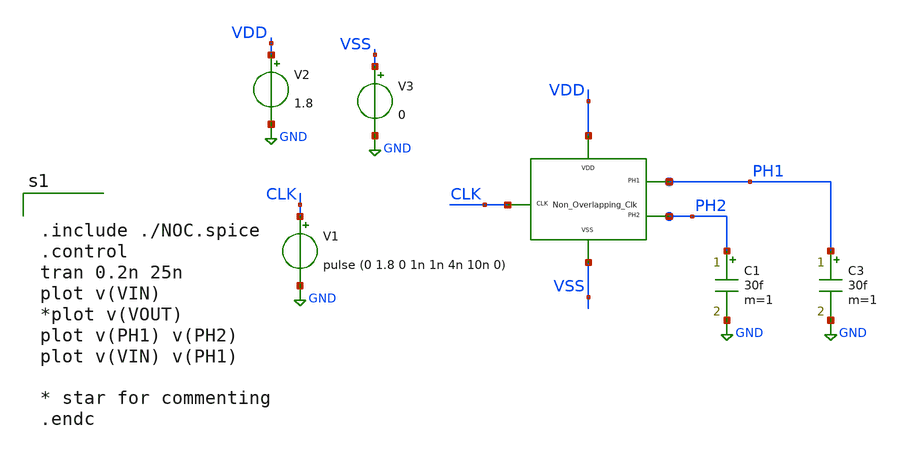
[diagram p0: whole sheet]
** sch_path: xschem/DC_DC_Converter_xschem/DC_DC_Converter/Non_Overlap_Clk/Non_over_clk_PEX_TB.sch
**.subckt Non_over_clk_PEX_TB
V1 CLK GND pulse (0 1.8 0 1n 1n 4n 10n 0)
V2 VDD GND 1.8
C3 PH1 GND 30f m=1
C1 PH2 GND 30f m=1
V3 VSS GND 0
XNOC1 VDD CLK PH1 VSS PH2 Non_over_clk_PEX
**** begin user architecture code


.include ./NOC.spice
.control
tran 0.2n 25n
plot v(VIN)
*plot v(VOUT)
plot v(PH1) v(PH2)
plot v(VIN) v(PH1)

* star for commenting
.endc


** opencircuitdesign pdks install
.lib $::SKYWATER_MODELS/sky130.lib.spice tt


**** end user architecture code
**.ends
.GLOBAL GND
.end
